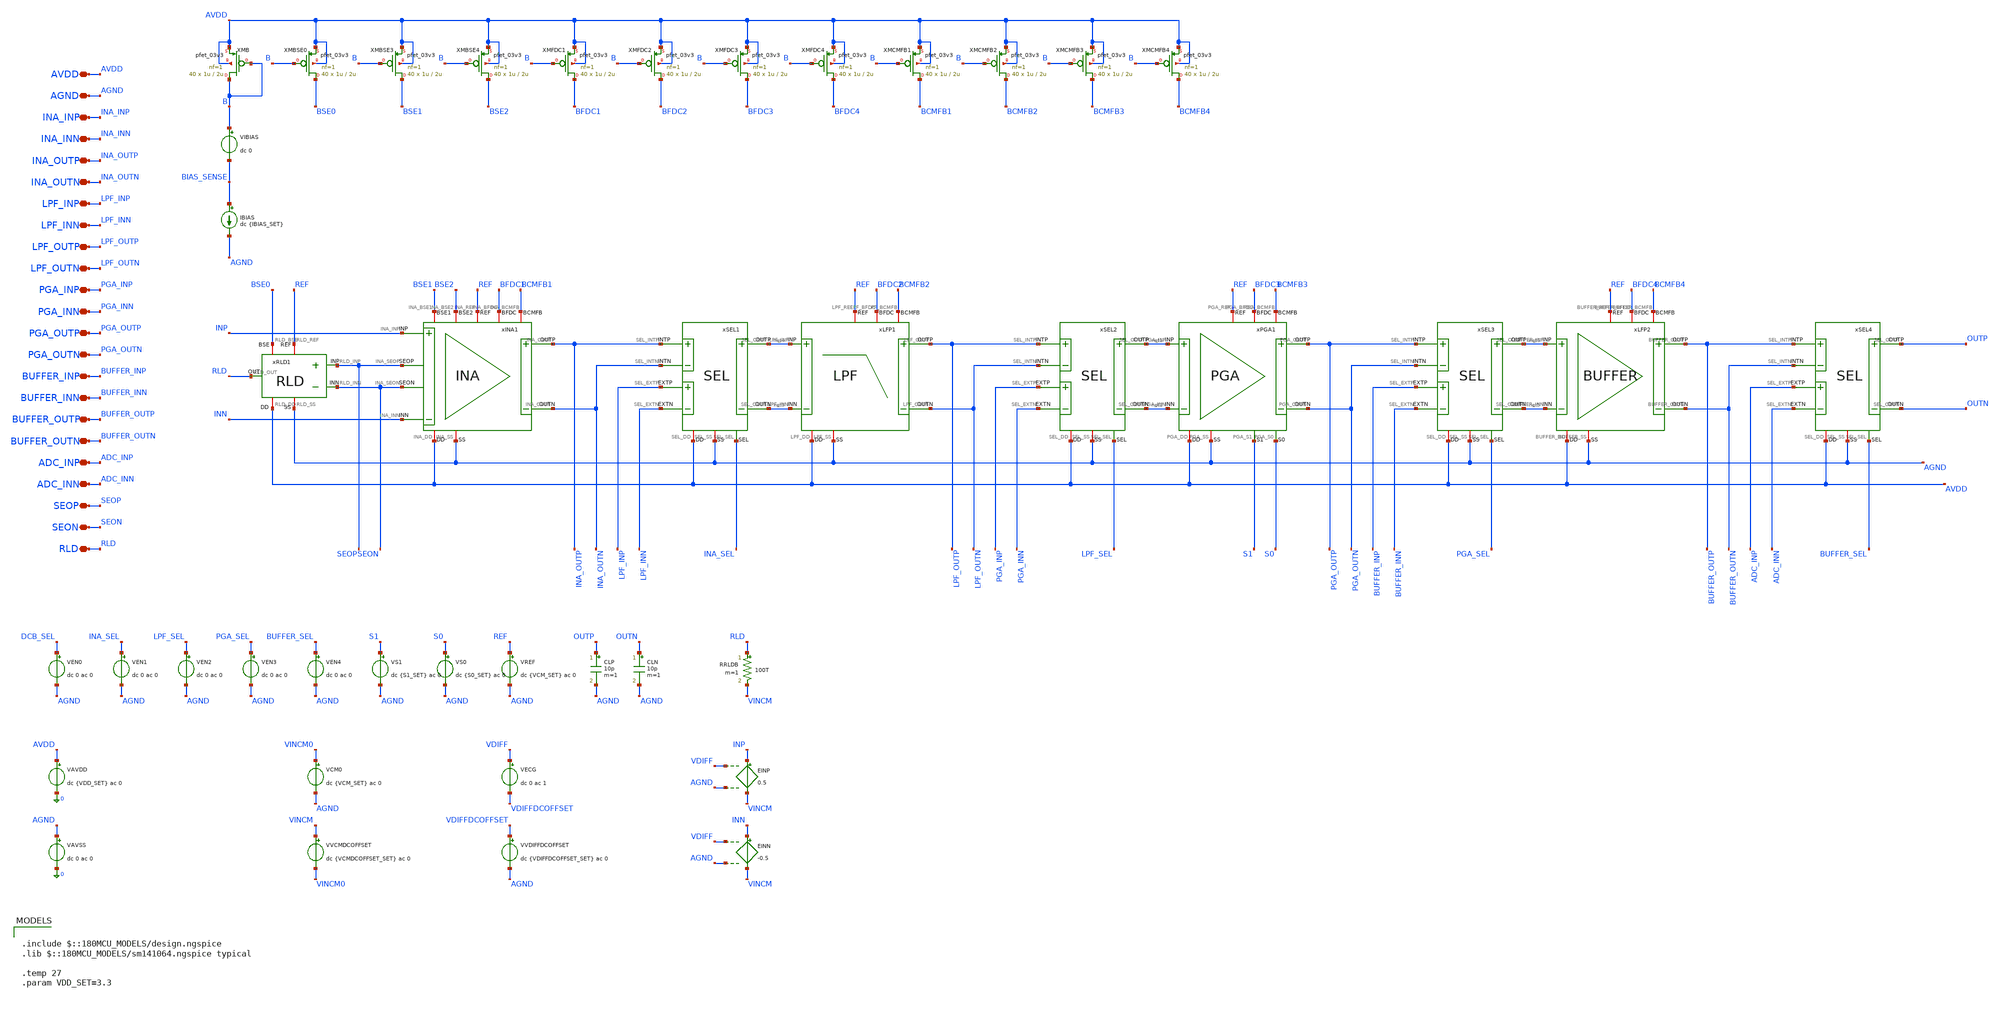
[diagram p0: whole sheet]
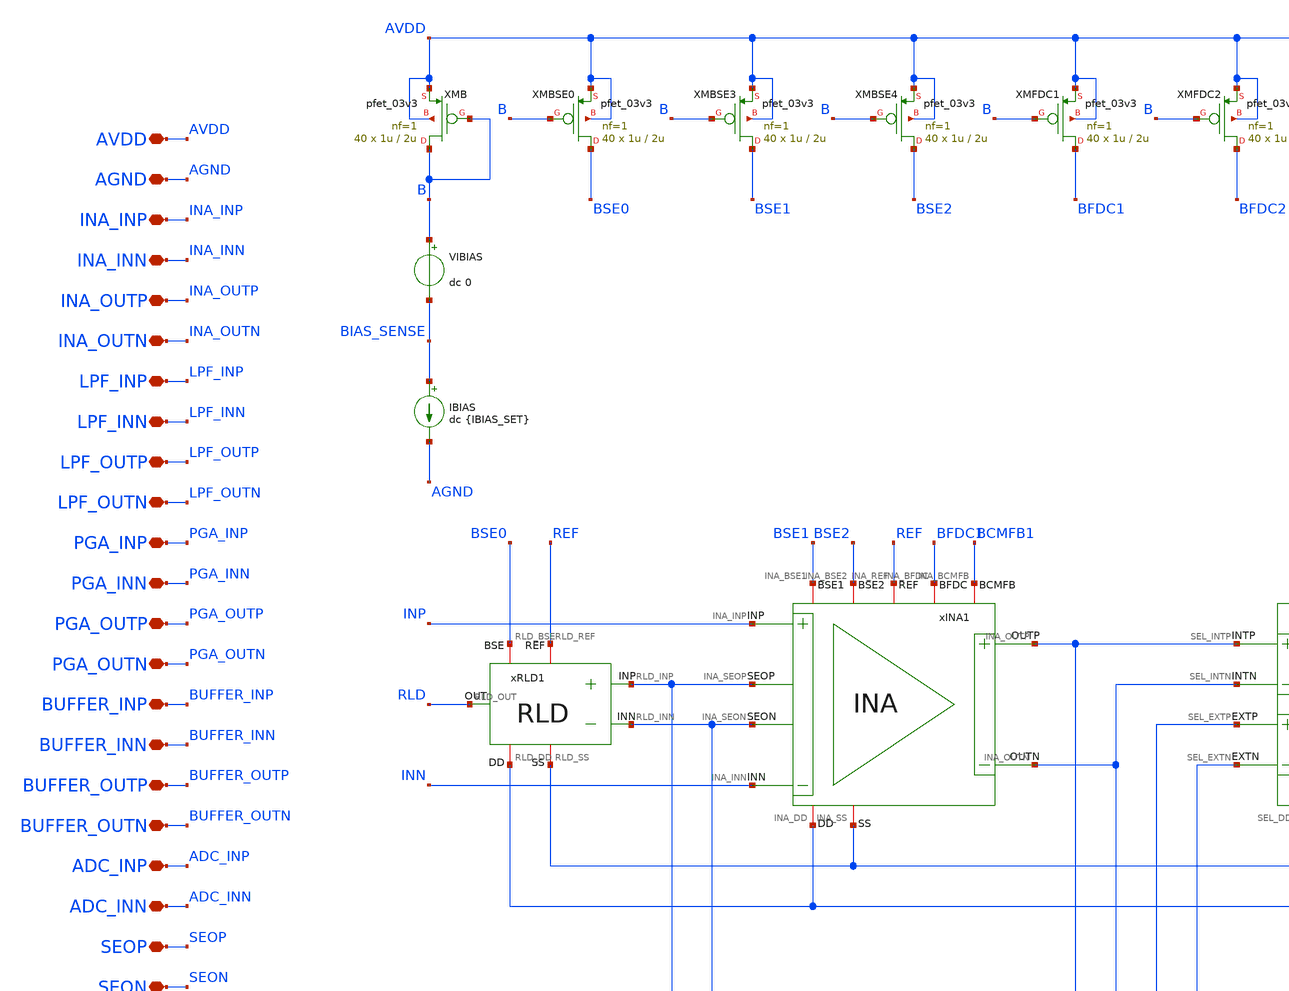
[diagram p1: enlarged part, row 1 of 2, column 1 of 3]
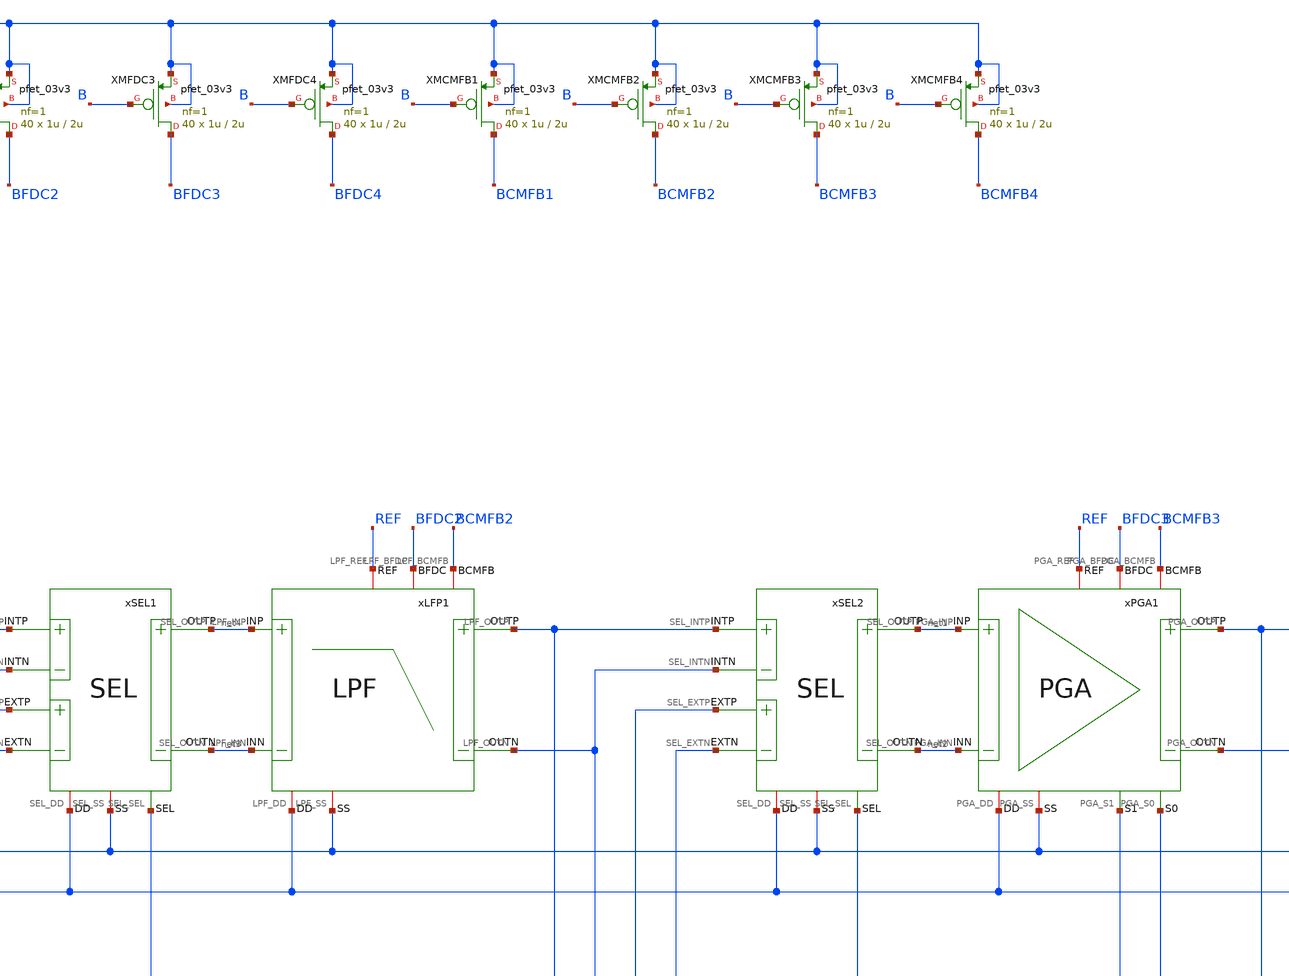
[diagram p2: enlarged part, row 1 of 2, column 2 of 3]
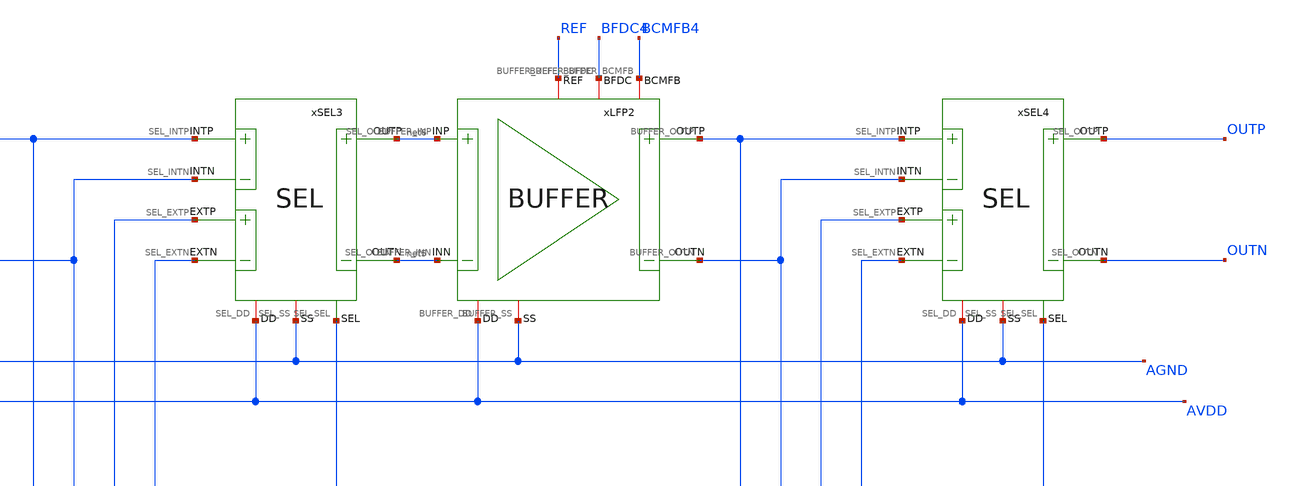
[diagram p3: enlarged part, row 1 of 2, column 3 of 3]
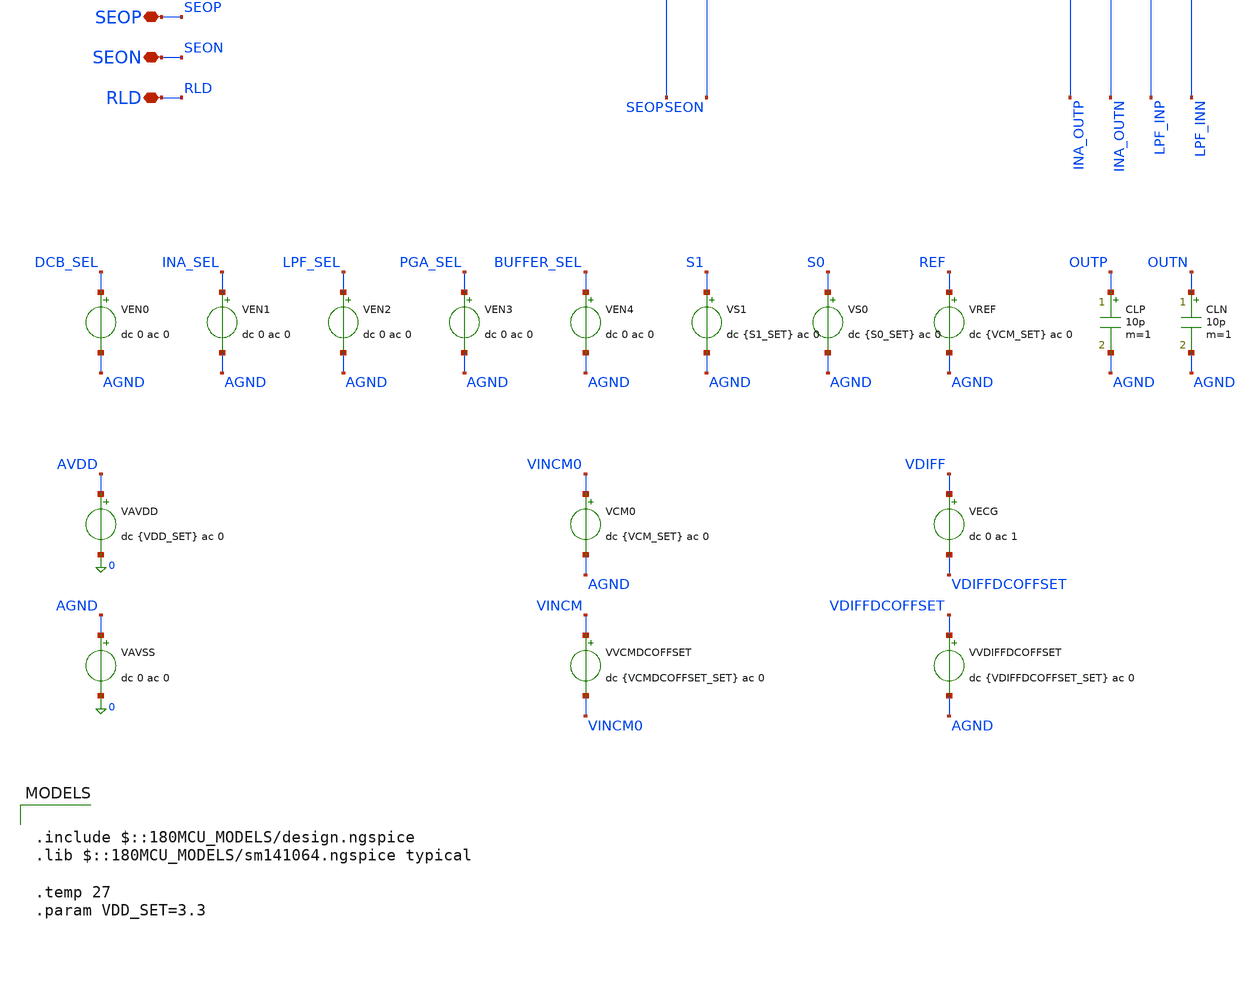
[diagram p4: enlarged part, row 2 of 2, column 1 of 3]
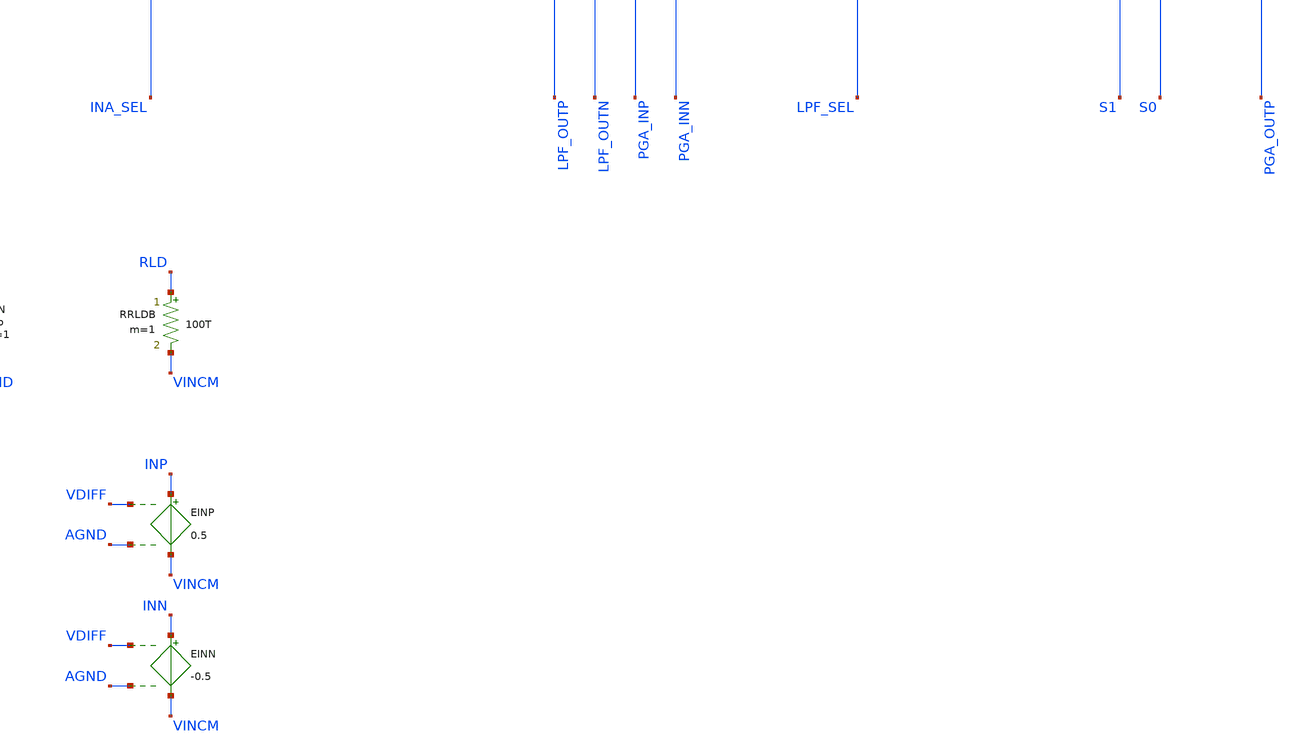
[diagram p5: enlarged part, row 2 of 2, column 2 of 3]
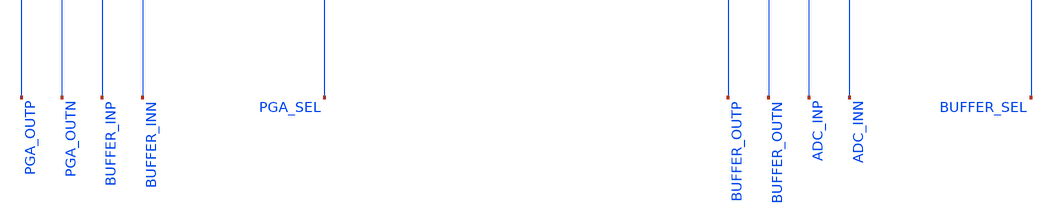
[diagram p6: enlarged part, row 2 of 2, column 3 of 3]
** sch_path: Design_Files/IC Design/Testbench/AFE/NOISE/AFE_TB_NOISE.sch
**.subckt AFE_TB_NOISE INA_INP INA_INN INA_OUTP INA_OUTN LPF_INP LPF_INN LPF_OUTP LPF_OUTN PGA_INP
*+ PGA_INN PGA_OUTP PGA_OUTN BUFFER_INP BUFFER_INN BUFFER_OUTP BUFFER_OUTN ADC_INP ADC_INN AVDD AGND SEOP SEON
*+ RLD
*.iopin INA_INP
*.iopin INA_INN
*.iopin INA_OUTP
*.iopin INA_OUTN
*.iopin LPF_INP
*.iopin LPF_INN
*.iopin LPF_OUTP
*.iopin LPF_OUTN
*.iopin PGA_INP
*.iopin PGA_INN
*.iopin PGA_OUTP
*.iopin PGA_OUTN
*.iopin BUFFER_INP
*.iopin BUFFER_INN
*.iopin BUFFER_OUTP
*.iopin BUFFER_OUTN
*.iopin ADC_INP
*.iopin ADC_INN
*.iopin AVDD
*.iopin AGND
*.iopin SEOP
*.iopin SEON
*.iopin RLD
CLP OUTP AGND 10p m=1
CLN OUTN AGND 10p m=1
VREF REF AGND dc {VCM_SET} ac 0
VEN1 INA_SEL AGND dc 0 ac 0
.save i(ven1)
VS0 S0 AGND dc {S0_SET} ac 0
VS1 S1 AGND dc {S1_SET} ac 0
VEN2 LPF_SEL AGND dc 0 ac 0
.save i(ven2)
VEN3 PGA_SEL AGND dc 0 ac 0
.save i(ven3)
VEN4 BUFFER_SEL AGND dc 0 ac 0
.save i(ven4)
VEN0 DCB_SEL AGND dc 0 ac 0
.save i(ven0)
VAVDD AVDD 0 dc {VDD_SET} ac 0
.save i(vavdd)
VAVSS AGND 0 dc 0 ac 0
.save i(vavss)
VCM0 VINCM0 AGND dc {VCM_SET} ac 0
VVCMDCOFFSET VINCM VINCM0 dc {VCMDCOFFSET_SET} ac 0
VECG VDIFF VDIFFDCOFFSET dc 0 ac 1
VVDIFFDCOFFSET VDIFFDCOFFSET AGND dc {VDIFFDCOFFSET_SET} ac 0
EINP INP VINCM VDIFF AGND 0.5
EINN INN VINCM VDIFF AGND -0.5
RRLDB RLD VINCM 100T m=1
VIBIAS B BIAS_SENSE dc 0
.save i(vibias)
IBIAS BIAS_SENSE AGND dc {IBIAS_SET}
xLFP1 AVDD AGND net4 net3 LPF_OUTN BFDC2 LPF_OUTP BCMFB2 REF LPF
xPGA1 AVDD AGND net1 net2 PGA_OUTN BFDC3 PGA_OUTP BCMFB3 REF S1 S0 PGA
xSEL1 AVDD AGND INA_OUTP INA_OUTN net3 net4 LPF_INP LPF_INN INA_SEL SEL
xINA1 AVDD AGND INP INN INA_OUTN BFDC1 INA_OUTP BCMFB1 REF SEON SEOP BSE1 BSE2 INA
xSEL2 AVDD AGND LPF_OUTP LPF_OUTN net2 net1 PGA_INP PGA_INN LPF_SEL SEL
xSEL3 AVDD AGND PGA_OUTP PGA_OUTN net5 net6 BUFFER_INP BUFFER_INN PGA_SEL SEL
xSEL4 AVDD AGND BUFFER_OUTP BUFFER_OUTN OUTN OUTP ADC_INP ADC_INN BUFFER_SEL SEL
xLFP2 AVDD AGND net6 net5 BUFFER_OUTN BFDC4 BUFFER_OUTP BCMFB4 REF BUFFER
XMB B B AVDD AVDD pfet_03v3 L=2u W=1u nf=1 ad='int((nf+1)/2) * W/nf * 0.18u' as='int((nf+2)/2) * W/nf * 0.18u'
+ pd='2*int((nf+1)/2) * (W/nf + 0.18u)' ps='2*int((nf+2)/2) * (W/nf + 0.18u)' nrd='0.18u / W' nrs='0.18u / W'
+ sa=0 sb=0 sd=0 m=40
XMBSE3 BSE1 B AVDD AVDD pfet_03v3 L=2u W=1u nf=1 ad='int((nf+1)/2) * W/nf * 0.18u' as='int((nf+2)/2) * W/nf * 0.18u'
+ pd='2*int((nf+1)/2) * (W/nf + 0.18u)' ps='2*int((nf+2)/2) * (W/nf + 0.18u)' nrd='0.18u / W' nrs='0.18u / W'
+ sa=0 sb=0 sd=0 m=40
XMBSE4 BSE2 B AVDD AVDD pfet_03v3 L=2u W=1u nf=1 ad='int((nf+1)/2) * W/nf * 0.18u' as='int((nf+2)/2) * W/nf * 0.18u'
+ pd='2*int((nf+1)/2) * (W/nf + 0.18u)' ps='2*int((nf+2)/2) * (W/nf + 0.18u)' nrd='0.18u / W' nrs='0.18u / W'
+ sa=0 sb=0 sd=0 m=40
XMFDC1 BFDC1 B AVDD AVDD pfet_03v3 L=2u W=1u nf=1 ad='int((nf+1)/2) * W/nf * 0.18u' as='int((nf+2)/2) * W/nf * 0.18u'
+ pd='2*int((nf+1)/2) * (W/nf + 0.18u)' ps='2*int((nf+2)/2) * (W/nf + 0.18u)' nrd='0.18u / W' nrs='0.18u / W'
+ sa=0 sb=0 sd=0 m=40
XMFDC2 BFDC2 B AVDD AVDD pfet_03v3 L=2u W=1u nf=1 ad='int((nf+1)/2) * W/nf * 0.18u' as='int((nf+2)/2) * W/nf * 0.18u'
+ pd='2*int((nf+1)/2) * (W/nf + 0.18u)' ps='2*int((nf+2)/2) * (W/nf + 0.18u)' nrd='0.18u / W' nrs='0.18u / W'
+ sa=0 sb=0 sd=0 m=40
XMFDC3 BFDC3 B AVDD AVDD pfet_03v3 L=2u W=1u nf=1 ad='int((nf+1)/2) * W/nf * 0.18u' as='int((nf+2)/2) * W/nf * 0.18u'
+ pd='2*int((nf+1)/2) * (W/nf + 0.18u)' ps='2*int((nf+2)/2) * (W/nf + 0.18u)' nrd='0.18u / W' nrs='0.18u / W'
+ sa=0 sb=0 sd=0 m=40
XMFDC4 BFDC4 B AVDD AVDD pfet_03v3 L=2u W=1u nf=1 ad='int((nf+1)/2) * W/nf * 0.18u' as='int((nf+2)/2) * W/nf * 0.18u'
+ pd='2*int((nf+1)/2) * (W/nf + 0.18u)' ps='2*int((nf+2)/2) * (W/nf + 0.18u)' nrd='0.18u / W' nrs='0.18u / W'
+ sa=0 sb=0 sd=0 m=40
XMCMFB1 BCMFB1 B AVDD AVDD pfet_03v3 L=2u W=1u nf=1 ad='int((nf+1)/2) * W/nf * 0.18u' as='int((nf+2)/2) * W/nf * 0.18u'
+ pd='2*int((nf+1)/2) * (W/nf + 0.18u)' ps='2*int((nf+2)/2) * (W/nf + 0.18u)' nrd='0.18u / W' nrs='0.18u / W'
+ sa=0 sb=0 sd=0 m=40
XMCMFB2 BCMFB2 B AVDD AVDD pfet_03v3 L=2u W=1u nf=1 ad='int((nf+1)/2) * W/nf * 0.18u' as='int((nf+2)/2) * W/nf * 0.18u'
+ pd='2*int((nf+1)/2) * (W/nf + 0.18u)' ps='2*int((nf+2)/2) * (W/nf + 0.18u)' nrd='0.18u / W' nrs='0.18u / W'
+ sa=0 sb=0 sd=0 m=40
XMCMFB3 BCMFB3 B AVDD AVDD pfet_03v3 L=2u W=1u nf=1 ad='int((nf+1)/2) * W/nf * 0.18u' as='int((nf+2)/2) * W/nf * 0.18u'
+ pd='2*int((nf+1)/2) * (W/nf + 0.18u)' ps='2*int((nf+2)/2) * (W/nf + 0.18u)' nrd='0.18u / W' nrs='0.18u / W'
+ sa=0 sb=0 sd=0 m=40
XMCMFB4 BCMFB4 B AVDD AVDD pfet_03v3 L=2u W=1u nf=1 ad='int((nf+1)/2) * W/nf * 0.18u' as='int((nf+2)/2) * W/nf * 0.18u'
+ pd='2*int((nf+1)/2) * (W/nf + 0.18u)' ps='2*int((nf+2)/2) * (W/nf + 0.18u)' nrd='0.18u / W' nrs='0.18u / W'
+ sa=0 sb=0 sd=0 m=40
XMBSE0 BSE0 B AVDD AVDD pfet_03v3 L=2u W=1u nf=1 ad='int((nf+1)/2) * W/nf * 0.18u' as='int((nf+2)/2) * W/nf * 0.18u'
+ pd='2*int((nf+1)/2) * (W/nf + 0.18u)' ps='2*int((nf+2)/2) * (W/nf + 0.18u)' nrd='0.18u / W' nrs='0.18u / W'
+ sa=0 sb=0 sd=0 m=40
xRLD1 AVDD AGND SEOP SEON RLD REF BSE0 RLD
**** begin user architecture code

.include $::180MCU_MODELS/design.ngspice
.lib $::180MCU_MODELS/sm141064.ngspice typical

.temp 27
.param VDD_SET=3.3



.param VCM_SET={VDD_SET/2}

.param VCMDCOFFSET_SET=0
.param VDIFFDCOFFSET_SET=0

.param IBIAS_SET=40u

.param S1_SET=3.3
.param S0_SET=3.3

.options sparse
.options method=gear

.options reltol=1e-3
.options abstol=1e-12
.options vntol=1u
.options chgtol=1e-14

.options itl1=2000
.options itl2=1000
.options itl4=2000

.options gmin=1e-12
.options rshunt=100T

.nodeset v(B)=2.3

.nodeset v(INP)={VCM_SET}
.nodeset v(INN)={VCM_SET}

.nodeset v(OUTP)={VCM_SET}
.nodeset v(OUTN)={VCM_SET}

.nodeset v(RLD)={VCM_SET}

.save all





.control

destroy all

set noaskquit
set wr_singlescale
unset wr_vecnames
set appendwrite

unset sqrnoise

option numdgt=15
option sparse

shell mkdir -p
+ /foss/designs/ECG_Acquisition_IC/Measurement_Results/IC_Simulation/PATH/NOM.Result_txt

shell rm -f
+ /foss/designs/ECG_Acquisition_IC/Measurement_Results/IC_Simulation/PATH/NOM.Result_txt/NOM.noise_diff.txt


* Differential noise: PGA G2 and G16
foreach gaincfg 0 1

    if $gaincfg = 0
        alterparam S1_SET=0
        alterparam S0_SET=0
    else
        alterparam S1_SET=3.3
        alterparam S0_SET=3.3
    end

    reset
    save all

    alter @VECG[ACMAG]=1
    alter @VECG[ACPHASE]=0

    alter @VCM0[ACMAG]=0
    alter @VCM0[ACPHASE]=0

    alter @VAVDD[ACMAG]=0
    alter @VAVDD[ACPHASE]=0

    alter @VAVSS[ACMAG]=0
    alter @VAVSS[ACPHASE]=0

    op

    noise v(OUTP,OUTN) VECG dec 300 0.01 1k

    * noise leaves the one-row integrated plot active
    * previous plot contains the noise-density spectrum
    setplot previous
    setscale frequency

    if $gaincfg = 0
        let noise_pga_gain=frequency*0+2
    else
        let noise_pga_gain=frequency*0+16
    end

    let noise_out_density=onoise_spectrum
    let noise_in_density=inoise_spectrum

    wrdata
+ /foss/designs/ECG_Acquisition_IC/Measurement_Results/IC_Simulation/PATH/NOM.Result_txt/NOM.noise_diff.txt noise_pga_gain noise_out_density noise_in_density

    destroy all

end


* Last simulated setting is PGA G16

quit
.endc


**** end user architecture code
**.ends
.end
